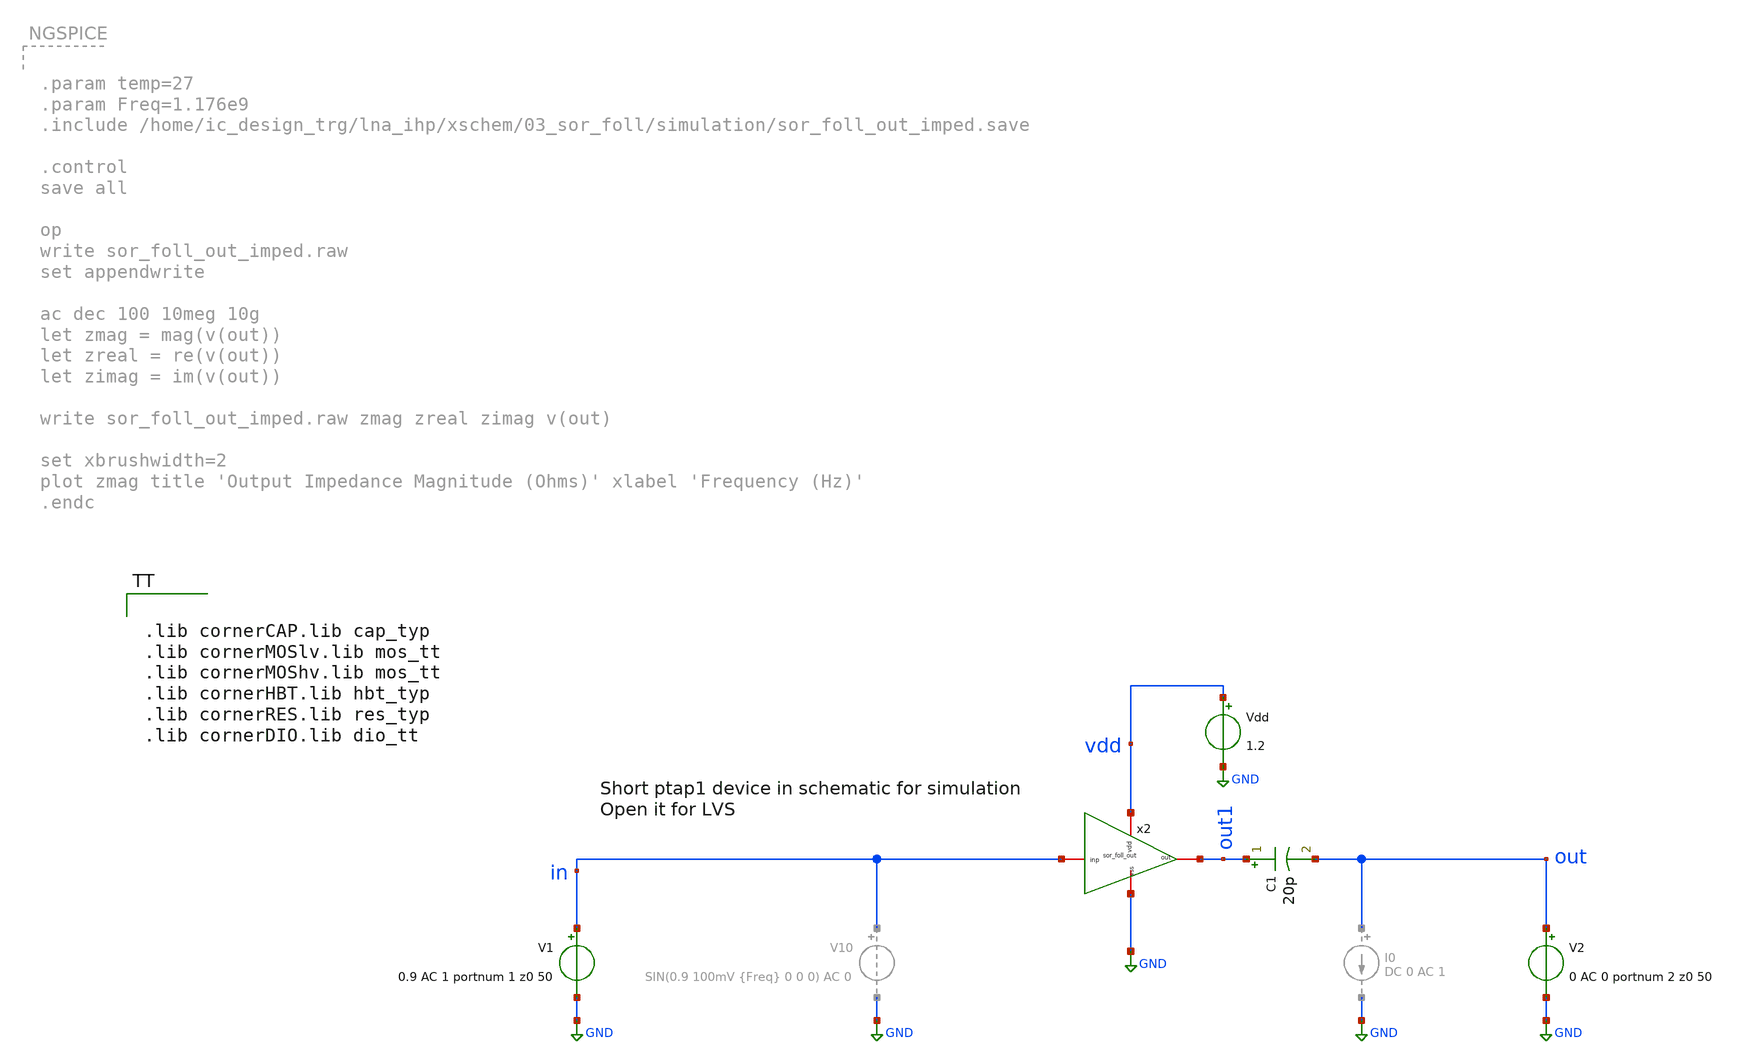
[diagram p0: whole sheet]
** sch_path: LNA7096-main/schematic/xschem/03_sor_foll/sor_foll_out_imped.sch
* Copyright 2023 IHP PDK Authors
**.subckt sor_foll_out_imped
Vdd vdd GND 1.2
V1 in GND 0.9 AC 1 portnum 1 z0 50
V2 out GND 0 AC 0 portnum 2 z0 50
C1 out1 out 20p m=1
x2 vdd in out1 GND sor_foll_out
**** begin user architecture code

.lib cornerCAP.lib cap_typ
.lib cornerMOSlv.lib mos_tt
.lib cornerMOShv.lib mos_tt
.lib cornerHBT.lib hbt_typ
.lib cornerRES.lib res_typ
.lib cornerDIO.lib dio_tt




.param temp=27
.param Freq=1.176e9
.include /home/ic_design_trg/lna_ihp/xschem/03_sor_foll/simulation/sor_foll_out_imped.save

.control
* --- 0. Setup and Initialization ---
* FORCE ngspice to keep all nodes and S-parameters in memory!
save all S_1_1 S_2_1 S_1_2 S_2_2

unset appendwrite

* --- 1. Operating Point Analysis (OP) ---
op
write sor_foll_out_imped.raw all
set appendwrite
destroy $curplot

* --- 2. AC Analysis ---
ac dec 100 10meg 10g
let zmag_ac = mag(v(out))
* [CORRECTED] Use real() and imag() instead of re() and im()
let zreal_ac = real(v(out))
let zimag_ac = imag(v(out))

* Write AC output impedance vectors to the RAW file
write sor_foll_out_imped.raw zmag_ac zreal_ac zimag_ac v(out)
set appendwrite


* Free up memory from AC plot
destroy $curplot

* --- 3. S-Parameter (SP) Analysis ---
sp dec 100 10meg 10g
let s11_db = db(S_1_1)
let s21_db = db(S_2_1)
let s12_db = db(S_1_2)
let s22_db = db(S_2_2)

* Calculate Output Impedance from S22
* Formula: Zout = Z0 * (1 + S22) / (1 - S22) where Z0 is your reference 50 Ohms
let zout_sp = 50 * (1 + S_2_2) / (1 - S_2_2)

* Extract Magnitude, Real, and Imaginary parts of the SP Output Impedance
let zmag_sp = mag(zout_sp)
* [CORRECTED] Use real() and imag() instead of re() and im()
let zreal_sp = real(zout_sp)
let zimag_sp = imag(zout_sp)

* Explicitly write ONLY the S-parameters and calculated impedance vectors to the RAW file
write sor_foll_out_imped.raw S_1_1 S_2_1 S_1_2 S_2_2 s11_db s21_db s12_db s22_db zout_sp zmag_sp
+ zreal_sp zimag_sp

* Plot S-Parameters natively
set xbrushwidth=2
plot s11_db s21_db s12_db s22_db title 'S-Parameters (dB)' ylabel 'Magnitude (dB)' xlabel 'Frequency (Hz)'

* Plot Output Impedance from SP Analysis natively
plot zmag_sp title 'SP Output Impedance Magnitude (Ohms)' ylabel 'Impedance (Ohms)' xlabel 'Frequency (Hz)'

* Free up memory from SP plot
destroy $curplot
.endc


**** end user architecture code
**.ends

* expanding   symbol:  03_sor_foll/sor_foll_out.sym # of pins=4
** sym_path: LNA7096-main/schematic/xschem/03_sor_foll/sor_foll_out.sym
** sch_path: LNA7096-main/schematic/xschem/03_sor_foll/sor_foll_out.sch
.subckt sor_foll_out vdd inp out vss
*.iopin vdd
*.iopin vss
*.iopin inp
*.iopin out
XR3 vdd n8 vss rhigh w=1e-6 l=5e-6 m=1 b=0 mm_ok=1
XM3 out n8 vss vss sg13_lv_nmos w=85.925u l=0.25u ng=35 m=1 mm_ok=1
XM2 n8 n8 vss vss sg13_lv_nmos w=5u l=0.25u ng=1 m=1 mm_ok=1
XM1 vdd inp out net1 sg13_lv_nmos w=184.86u l=0.25u ng=20 m=1 mm_ok=1
XD1 net1 vdd vss isolbox l=29.14u w=10.735u
XR1 out net1 ptap1 R=55.97 w=0.39e-6 l=7e-6
.ends

.GLOBAL GND
.end
